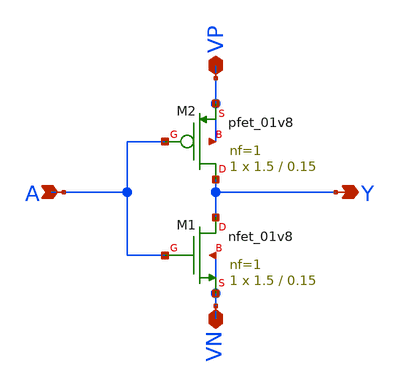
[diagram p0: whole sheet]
** sch_path: week 0/sim/pre-layout/inverter.sch
**.subckt inverter VN VP A Y
*.iopin VN
*.iopin VP
*.ipin A
*.opin Y
XM1 Y A VN VN sky130_fd_pr__nfet_01v8 L=0.15 W=1.5 nf=1 ad='int((nf+1)/2) * W/nf * 0.29' as='int((nf+2)/2) * W/nf * 0.29'
+ pd='2*int((nf+1)/2) * (W/nf + 0.29)' ps='2*int((nf+2)/2) * (W/nf + 0.29)' nrd='0.29 / W' nrs='0.29 / W'
+ sa=0 sb=0 sd=0 mult=1 m=1
XM2 Y A VP VP sky130_fd_pr__pfet_01v8 L=0.15 W=1.5 nf=1 ad='int((nf+1)/2) * W/nf * 0.29' as='int((nf+2)/2) * W/nf * 0.29'
+ pd='2*int((nf+1)/2) * (W/nf + 0.29)' ps='2*int((nf+2)/2) * (W/nf + 0.29)' nrd='0.29 / W' nrs='0.29 / W'
+ sa=0 sb=0 sd=0 mult=1 m=1
**.ends
.end
